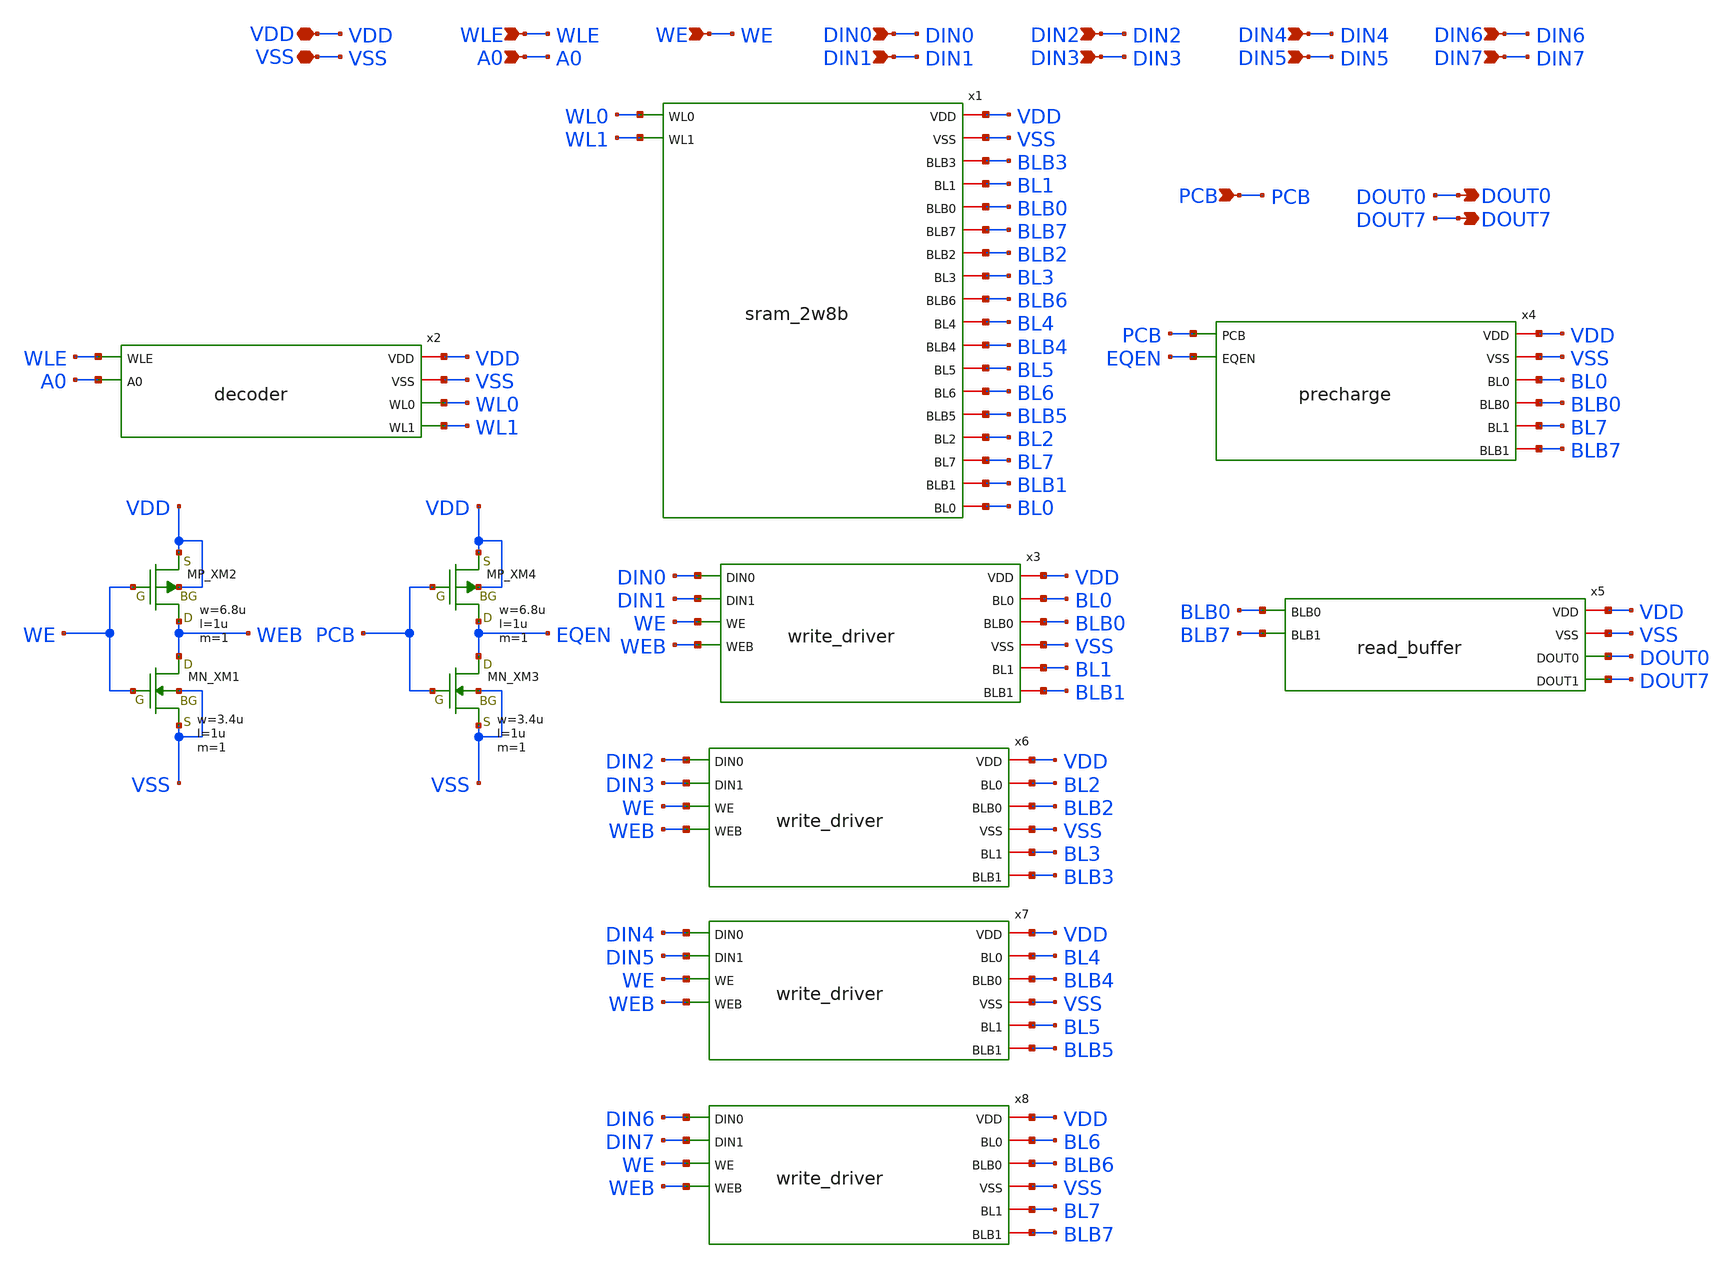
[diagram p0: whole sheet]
** sch_path: sram/sram_2w8b_top.sch
**.subckt sram_2w8b_top VDD WLE DOUT0 VSS A0 WE DIN0 DIN1 PCB DOUT7 DIN2 DIN3 DIN4 DIN5 DIN6 DIN7
*.iopin VDD
*.ipin WLE
*.opin DOUT0
*.iopin VSS
*.ipin A0
*.ipin WE
*.ipin DIN0
*.ipin DIN1
*.ipin PCB
*.opin DOUT7
*.ipin DIN2
*.ipin DIN3
*.ipin DIN4
*.ipin DIN5
*.ipin DIN6
*.ipin DIN7
x2 VDD VSS WL0 WLE A0 WL1 decoder
x3 DIN0 VDD BL0 BLB0 VSS DIN1 BL1 WE BLB1 WEB write_driver
x4 VDD VSS PCB EQEN BL0 BLB0 BL7 BLB7 precharge
x5 VDD VSS BLB0 BLB7 DOUT0 DOUT7 read_buffer
XXM1 WEB WE VSS VSS NMOS w=3.4u l=1u nrd=0 nrs=0 m=1
XXM2 WEB WE VDD VDD PMOS w=6.8u l=1u nrd=0 nrs=0 m=1
XXM3 EQEN PCB VSS VSS NMOS w=3.4u l=1u nrd=0 nrs=0 m=1
XXM4 EQEN PCB VDD VDD PMOS w=6.8u l=1u nrd=0 nrs=0 m=1
x6 DIN2 VDD BL2 BLB2 VSS DIN3 BL3 WE BLB3 WEB write_driver
x7 DIN4 VDD BL4 BLB4 VSS DIN5 BL5 WE BLB5 WEB write_driver
x8 DIN6 VDD BL6 BLB6 VSS DIN7 BL7 WE BLB7 WEB write_driver
x1 WL0 VDD VSS WL1 BLB3 BL1 BLB0 BLB7 BLB2 BL3 BLB6 BL4 BLB4 BL5 BL6 BLB5 BL2 BL7 BLB1 BL0 sram_2w8b
**.ends
.end
